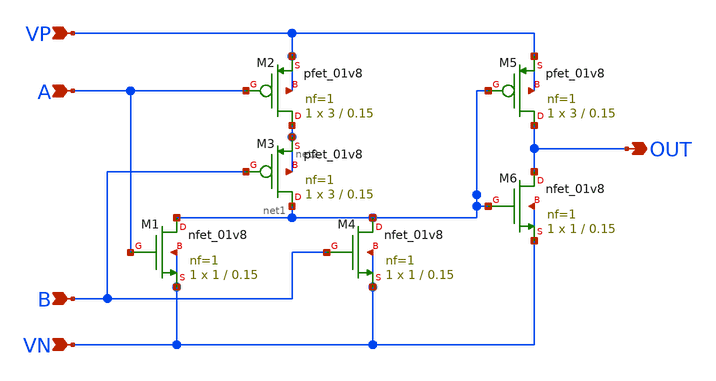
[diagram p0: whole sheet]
** sch_path: APIC-3/schematic/or_gate/or_gate.sch
**.subckt or_gate A B OUT VP VN
*.ipin A
*.ipin B
*.opin OUT
*.ipin VP
*.ipin VN
XM1 net1 A VN VN sky130_fd_pr__nfet_01v8 L=0.15 W=1 nf=1 ad='int((nf+1)/2) * W/nf * 0.29' as='int((nf+2)/2) * W/nf * 0.29'
+ pd='2*int((nf+1)/2) * (W/nf + 0.29)' ps='2*int((nf+2)/2) * (W/nf + 0.29)' nrd='0.29 / W' nrs='0.29 / W'
+ sa=0 sb=0 sd=0 mult=1 m=1
XM4 net1 B VN VN sky130_fd_pr__nfet_01v8 L=0.15 W=1 nf=1 ad='int((nf+1)/2) * W/nf * 0.29' as='int((nf+2)/2) * W/nf * 0.29'
+ pd='2*int((nf+1)/2) * (W/nf + 0.29)' ps='2*int((nf+2)/2) * (W/nf + 0.29)' nrd='0.29 / W' nrs='0.29 / W'
+ sa=0 sb=0 sd=0 mult=1 m=1
XM6 OUT net1 VN VN sky130_fd_pr__nfet_01v8 L=0.15 W=1 nf=1 ad='int((nf+1)/2) * W/nf * 0.29' as='int((nf+2)/2) * W/nf * 0.29'
+ pd='2*int((nf+1)/2) * (W/nf + 0.29)' ps='2*int((nf+2)/2) * (W/nf + 0.29)' nrd='0.29 / W' nrs='0.29 / W'
+ sa=0 sb=0 sd=0 mult=1 m=1
XM2 net2 A VP VP sky130_fd_pr__pfet_01v8 L=0.15 W=3 nf=1 ad='int((nf+1)/2) * W/nf * 0.29' as='int((nf+2)/2) * W/nf * 0.29'
+ pd='2*int((nf+1)/2) * (W/nf + 0.29)' ps='2*int((nf+2)/2) * (W/nf + 0.29)' nrd='0.29 / W' nrs='0.29 / W'
+ sa=0 sb=0 sd=0 mult=1 m=1
XM3 net1 B net2 net2 sky130_fd_pr__pfet_01v8 L=0.15 W=3 nf=1 ad='int((nf+1)/2) * W/nf * 0.29' as='int((nf+2)/2) * W/nf * 0.29'
+ pd='2*int((nf+1)/2) * (W/nf + 0.29)' ps='2*int((nf+2)/2) * (W/nf + 0.29)' nrd='0.29 / W' nrs='0.29 / W'
+ sa=0 sb=0 sd=0 mult=1 m=1
XM5 OUT net1 VP VP sky130_fd_pr__pfet_01v8 L=0.15 W=3 nf=1 ad='int((nf+1)/2) * W/nf * 0.29' as='int((nf+2)/2) * W/nf * 0.29'
+ pd='2*int((nf+1)/2) * (W/nf + 0.29)' ps='2*int((nf+2)/2) * (W/nf + 0.29)' nrd='0.29 / W' nrs='0.29 / W'
+ sa=0 sb=0 sd=0 mult=1 m=1
**.ends
.end
